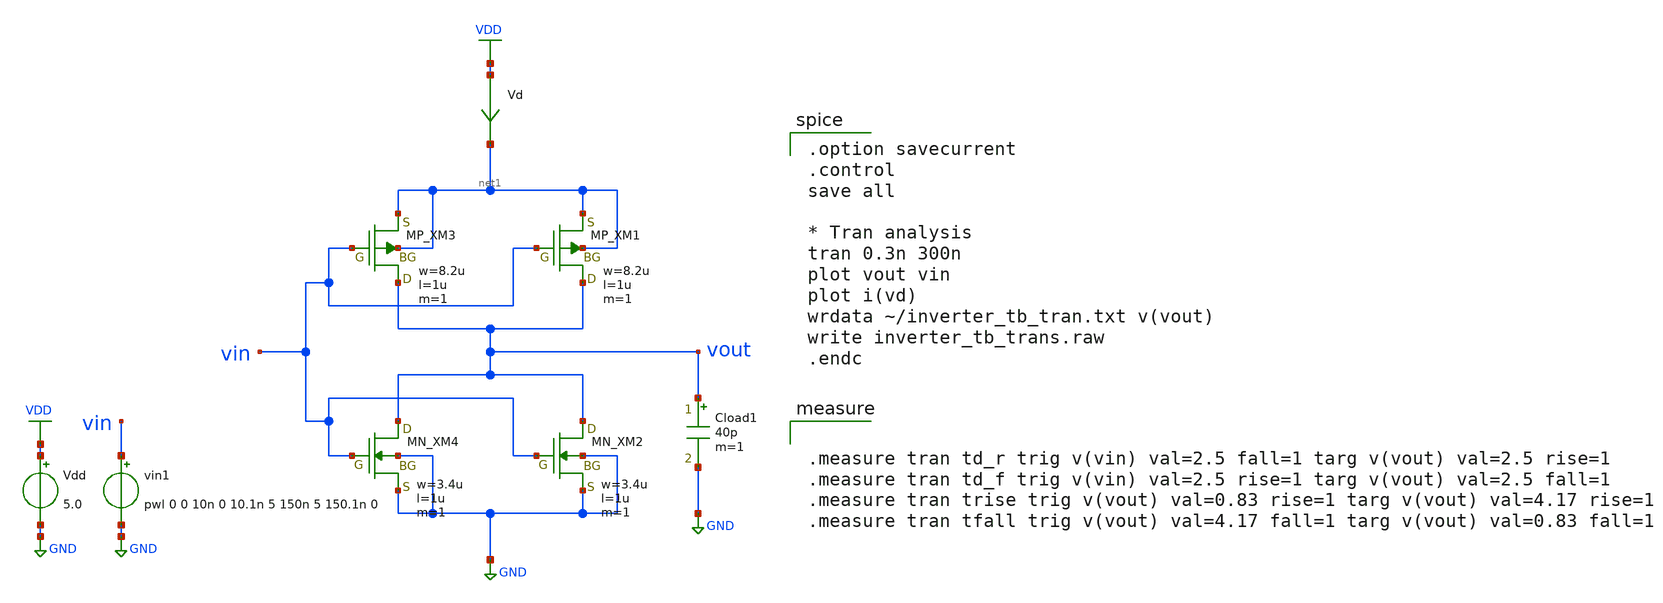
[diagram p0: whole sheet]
** sch_path: member_project/inverter/RISE-A/Talkie_junk/inverter_tb_trans.sch
**.subckt inverter_tb_trans
XXM1 vout vin net1 net1 PMOS w=8.2u l=1u nrd=0 nrs=0 m=1
XXM2 vout vin GND GND NMOS w=3.4u l=1u nrd=0 nrs=0 m=1
XXM3 vout vin net1 net1 PMOS w=8.2u l=1u nrd=0 nrs=0 m=1
XXM4 vout vin GND GND NMOS w=3.4u l=1u nrd=0 nrs=0 m=1
Vdd VDD GND 5.0
Vd VDD net1 0
.save i(vd)
Cload1 vout GND 40p m=1
vin1 vin GND pwl 0 0 10n 0 10.1n 5 150n 5 150.1n 0
**** begin user architecture code
 .include $::LIB/ip62_models

.option savecurrent
.control
save all

* Tran analysis
tran 0.3n 300n
plot vout vin
plot i(vd)
wrdata ~/inverter_tb_tran.txt v(vout)
write inverter_tb_trans.raw
.endc



.measure tran td_r trig v(vin) val=2.5 fall=1 targ v(vout) val=2.5 rise=1
.measure tran td_f trig v(vin) val=2.5 rise=1 targ v(vout) val=2.5 fall=1
.measure tran trise trig v(vout) val=0.83 rise=1 targ v(vout) val=4.17 rise=1
.measure tran tfall trig v(vout) val=4.17 fall=1 targ v(vout) val=0.83 fall=1


**** end user architecture code
**.ends
.GLOBAL VDD
.GLOBAL GND
.end
